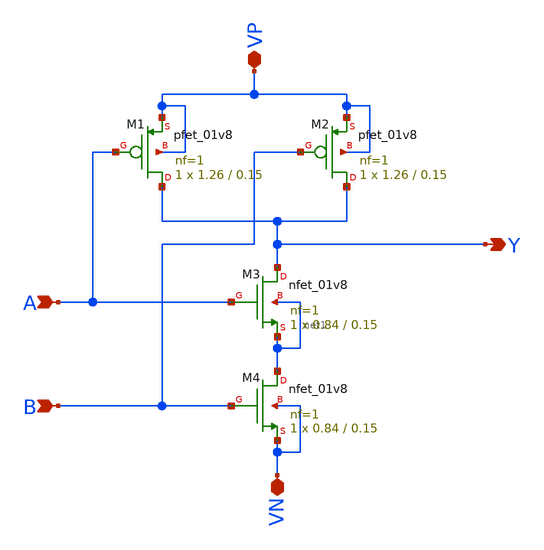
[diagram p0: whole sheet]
** sch_path: component/NAND2/NAND.sch
**.subckt NAND VP A B Y VN
*.iopin VP
*.ipin A
*.ipin B
*.opin Y
*.iopin VN
XM1 Y A VP VP sky130_fd_pr__pfet_01v8 L=0.15 W=1.26 nf=1 ad='int((nf+1)/2) * W/nf * 0.29' as='int((nf+2)/2) * W/nf * 0.29'
+ pd='2*int((nf+1)/2) * (W/nf + 0.29)' ps='2*int((nf+2)/2) * (W/nf + 0.29)' nrd='0.29 / W' nrs='0.29 / W'
+ sa=0 sb=0 sd=0 mult=1 m=1
XM2 Y B VP VP sky130_fd_pr__pfet_01v8 L=0.15 W=1.26 nf=1 ad='int((nf+1)/2) * W/nf * 0.29' as='int((nf+2)/2) * W/nf * 0.29'
+ pd='2*int((nf+1)/2) * (W/nf + 0.29)' ps='2*int((nf+2)/2) * (W/nf + 0.29)' nrd='0.29 / W' nrs='0.29 / W'
+ sa=0 sb=0 sd=0 mult=1 m=1
XM3 Y A net1 net1 sky130_fd_pr__nfet_01v8 L=0.15 W=0.84 nf=1 ad='int((nf+1)/2) * W/nf * 0.29' as='int((nf+2)/2) * W/nf * 0.29'
+ pd='2*int((nf+1)/2) * (W/nf + 0.29)' ps='2*int((nf+2)/2) * (W/nf + 0.29)' nrd='0.29 / W' nrs='0.29 / W'
+ sa=0 sb=0 sd=0 mult=1 m=1
XM4 net1 B VN VN sky130_fd_pr__nfet_01v8 L=0.15 W=0.84 nf=1 ad='int((nf+1)/2) * W/nf * 0.29' as='int((nf+2)/2) * W/nf * 0.29'
+ pd='2*int((nf+1)/2) * (W/nf + 0.29)' ps='2*int((nf+2)/2) * (W/nf + 0.29)' nrd='0.29 / W' nrs='0.29 / W'
+ sa=0 sb=0 sd=0 mult=1 m=1
**.ends
.end
